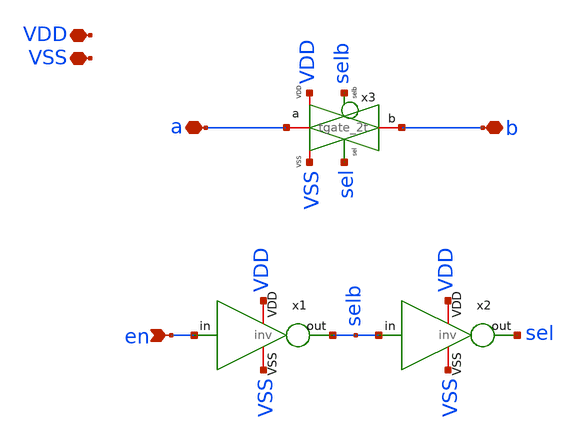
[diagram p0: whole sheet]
** sch_path: xsch/ip/tgate/tgate_6t.sch
**.subckt tgate_6t a b en VDD VSS
*.iopin a
*.iopin b
*.ipin en
*.iopin VDD
*.iopin VSS
x1 en selb VDD VSS inv
x2 selb sel VDD VSS inv
x3 a b sel selb VDD VSS tgate_2t
**.ends

* expanding   symbol:  ip/inv/inv.sym # of pins=4
** sym_path: xsch/ip/inv/inv.sym
** sch_path: xsch/ip/inv/inv.sch
.subckt inv in out VDD VSS
*.ipin in
*.opin out
*.iopin VDD
*.iopin VSS
XMN out in VSS VSS sky130_fd_pr__nfet_01v8 L=0.15 W=1 nf=1 ad='int((1 + 1)/2) * 1 / 1 * 0.29' as='int((1 + 2)/2) * 1 / 1 * 0.29'
+ pd='2*int((1 + 1)/2) * (1 / 1 + 0.29)' ps='2*int((1 + 2)/2) * (1 / 1 + 0.29)' nrd='0.29 / 1 ' nrs='0.29 / 1 '
+ sa=0 sb=0 sd=0 mult=1 m=1
XMP out in VDD VDD sky130_fd_pr__pfet_01v8 L=0.15 W=2 nf=1 ad='int((nf+1)/2) * W/nf * 0.29' as='int((nf+2)/2) * W/nf * 0.29'
+ pd='2*int((nf+1)/2) * (W/nf + 0.29)' ps='2*int((nf+2)/2) * (W/nf + 0.29)' nrd='0.29 / W' nrs='0.29 / W'
+ sa=0 sb=0 sd=0 mult=1 m=1
.ends


* expanding   symbol:  ip/tgate/tgate_2t.sym # of pins=6
** sym_path: xsch/ip/tgate/tgate_2t.sym
** sch_path: xsch/ip/tgate/tgate_2t.sch
.subckt tgate_2t a b sel selb VDD VSS
*.iopin a
*.iopin b
*.iopin VDD
*.iopin VSS
*.ipin sel
*.ipin selb
XMP a selb b VDD sky130_fd_pr__pfet_01v8 L=0.15 W=2 nf=1 ad='int((nf+1)/2) * W/nf * 0.29' as='int((nf+2)/2) * W/nf * 0.29'
+ pd='2*int((nf+1)/2) * (W/nf + 0.29)' ps='2*int((nf+2)/2) * (W/nf + 0.29)' nrd='0.29 / W' nrs='0.29 / W'
+ sa=0 sb=0 sd=0 mult=1 m=1
XMN a sel b VSS sky130_fd_pr__nfet_01v8 L=0.15 W=1 nf=1 ad='int((1 + 1)/2) * 1 / 1 * 0.29' as='int((1 + 2)/2) * 1 / 1 * 0.29'
+ pd='2*int((1 + 1)/2) * (1 / 1 + 0.29)' ps='2*int((1 + 2)/2) * (1 / 1 + 0.29)' nrd='0.29 / 1 ' nrs='0.29 / 1 '
+ sa=0 sb=0 sd=0 mult=1 m=1
.ends

.end
